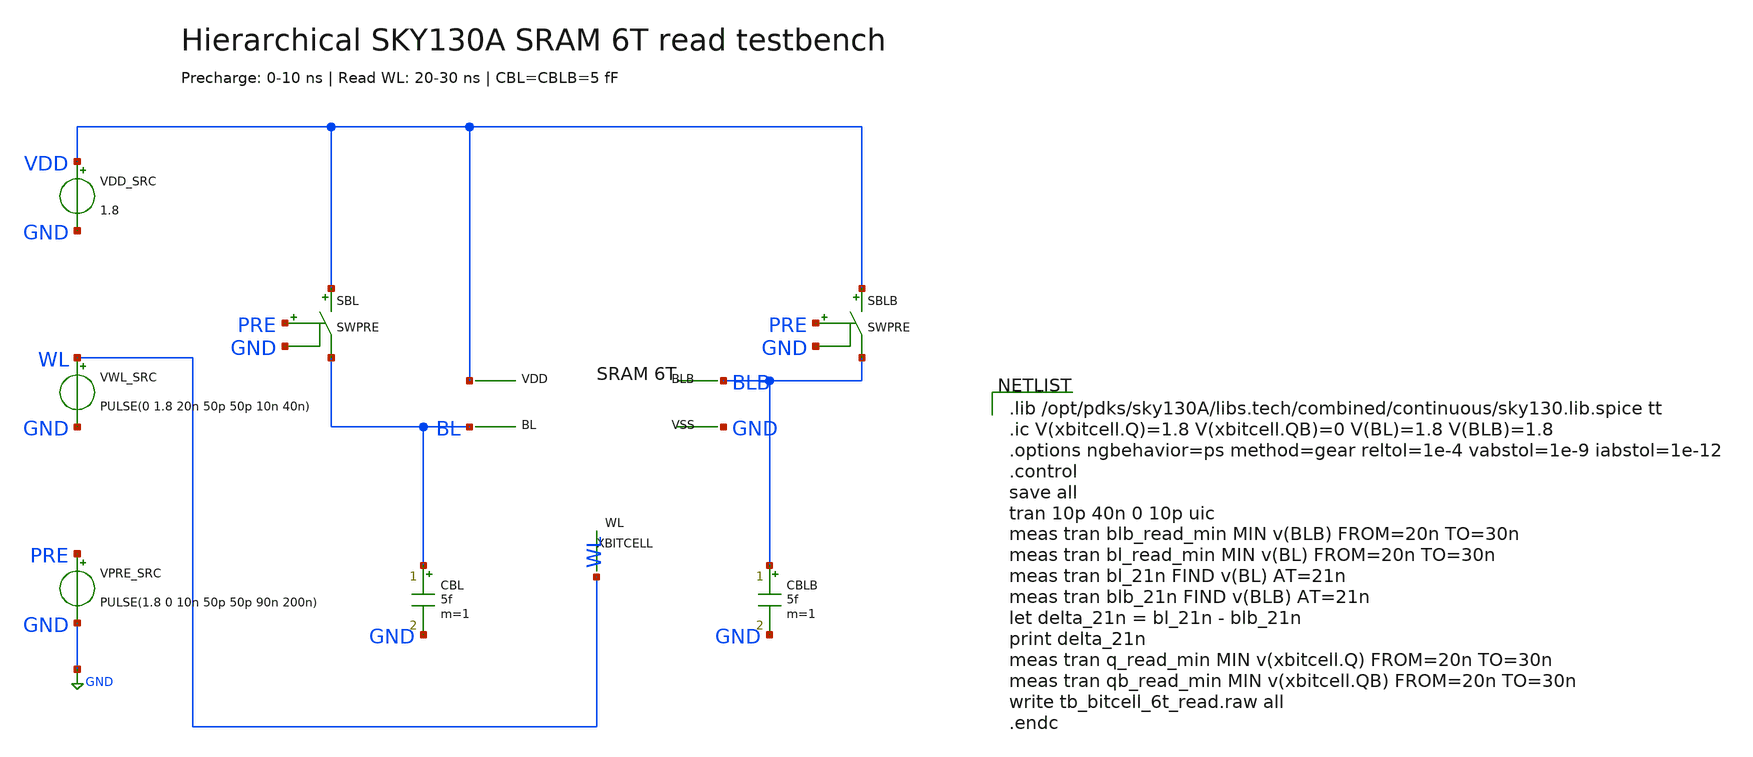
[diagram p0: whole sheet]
** sch_path: cells/tb_bitcell_6t_read.sch
**.subckt tb_bitcell_6t_read
XBITCELL VDD BL BLB GND WL bitcell_6t WPU=0.42 WPD=0.42 WACC=0.42
VDD_SRC VDD GND 1.8
VWL_SRC WL GND PULSE(0 1.8 20n 50p 50p 10n 40n)
VPRE_SRC PRE GND PULSE(1.8 0 10n 50p 50p 90n 200n)
SBL VDD BL PRE GND SWPRE
SBLB VDD BLB PRE GND SWPRE
CBL BL GND 5f m=1
CBLB BLB GND 5f m=1
**** begin user architecture code

.lib /opt/pdks/sky130A/libs.tech/combined/continuous/sky130.lib.spice tt
.ic V(xbitcell.Q)=1.8 V(xbitcell.QB)=0 V(BL)=1.8 V(BLB)=1.8
.options ngbehavior=ps method=gear reltol=1e-4 vabstol=1e-9 iabstol=1e-12
.control
save all
tran 10p 40n 0 10p uic
meas tran blb_read_min MIN v(BLB) FROM=20n TO=30n
meas tran bl_read_min MIN v(BL) FROM=20n TO=30n
meas tran bl_21n FIND v(BL) AT=21n
meas tran blb_21n FIND v(BLB) AT=21n
let delta_21n = bl_21n - blb_21n
print delta_21n
meas tran q_read_min MIN v(xbitcell.Q) FROM=20n TO=30n
meas tran qb_read_min MIN v(xbitcell.QB) FROM=20n TO=30n
write tb_bitcell_6t_read.raw all
.endc

**** end user architecture code
**.ends

* expanding   symbol:  cells/bitcell_6t.sym # of pins=5
** sym_path: cells/bitcell_6t.sym
** sch_path: cells/bitcell_6t.sch
.subckt bitcell_6t VDD BL BLB VSS WL  WPU=0.42 WPD=0.84 WACC=0.60
*.iopin VDD
*.iopin BL
*.iopin BLB
*.iopin VSS
*.iopin WL
XMPL Q QB VDD VDD sky130_fd_pr__pfet_01v8 L=0.15 W='WPU' nf=1 ad='W * 0.29' as='W * 0.29' pd='W + 2 * 0.29'
+ ps='W + 2 * 0.29' nrd=0 nrs=0 sa=0 sb=0 sd=0 mult=1 m=1
XMNL Q QB VSS VSS sky130_fd_pr__nfet_01v8 L=0.15 W='WPD' nf=1 ad='W * 0.29' as='W * 0.29' pd='W + 2 * 0.29'
+ ps='W + 2 * 0.29' nrd=0 nrs=0 sa=0 sb=0 sd=0 mult=1 m=1
XMPR QB Q VDD VDD sky130_fd_pr__pfet_01v8 L=0.15 W='WPU' nf=1 ad='W * 0.29' as='W * 0.29' pd='W + 2 * 0.29'
+ ps='W + 2 * 0.29' nrd=0 nrs=0 sa=0 sb=0 sd=0 mult=1 m=1
XMNR QB Q VSS VSS sky130_fd_pr__nfet_01v8 L=0.15 W='WPD' nf=1 ad='W * 0.29' as='W * 0.29' pd='W + 2 * 0.29'
+ ps='W + 2 * 0.29' nrd=0 nrs=0 sa=0 sb=0 sd=0 mult=1 m=1
XMAL Q WL BL VSS sky130_fd_pr__nfet_01v8 L=0.15 W='WACC' nf=1 ad='W * 0.29' as='W * 0.29' pd='W + 2 * 0.29'
+ ps='W + 2 * 0.29' nrd=0 nrs=0 sa=0 sb=0 sd=0 mult=1 m=1
XMAR BLB WL QB VSS sky130_fd_pr__nfet_01v8 L=0.15 W='WACC' nf=1 ad='W * 0.29' as='W * 0.29' pd='W + 2 * 0.29'
+ ps='W + 2 * 0.29' nrd=0 nrs=0 sa=0 sb=0 sd=0 mult=1 m=1
.ends

.GLOBAL GND
**** begin user architecture code
.model SWPRE SW(RON=10 ROFF=1e12 VT=0.9 VH=0.1)
**** end user architecture code
.end
